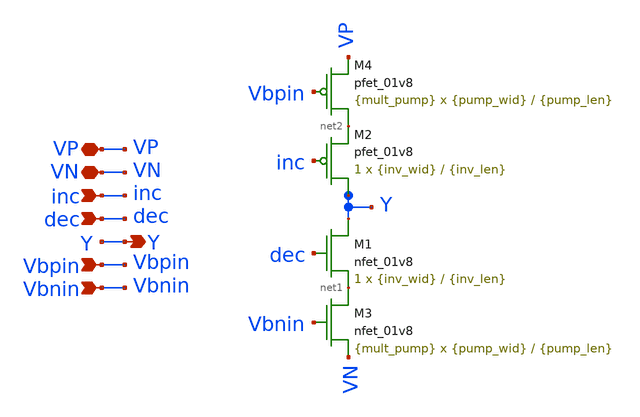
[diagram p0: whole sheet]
** sch_path: ipump.sch
**.subckt ipump VN VP Y Vbpin inc Vbnin dec
*.iopin VN
*.iopin VP
*.opin Y
*.ipin Vbpin
*.ipin inc
*.ipin Vbnin
*.ipin dec
XM1 Y dec net1 VN sky130_fd_pr__nfet_01v8 L={inv_len} W={inv_wid} nf=1 ad='int((nf+1)/2) * W/nf * 0.29'
+ as='int((nf+2)/2) * W/nf * 0.29' pd='2*int((nf+1)/2) * (W/nf + 0.29)' ps='2*int((nf+2)/2) * (W/nf + 0.29)'
+ nrd='0.29 / W' nrs='0.29 / W' sa=0 sb=0 sd=0 mult=1 m=1
XM2 Y inc net2 VP sky130_fd_pr__pfet_01v8 L={inv_len} W={inv_wid} nf=1 ad='int((nf+1)/2) * W/nf * 0.29'
+ as='int((nf+2)/2) * W/nf * 0.29' pd='2*int((nf+1)/2) * (W/nf + 0.29)' ps='2*int((nf+2)/2) * (W/nf + 0.29)'
+ nrd='0.29 / W' nrs='0.29 / W' sa=0 sb=0 sd=0 mult=1 m=1
XM3 net1 Vbnin VN VN sky130_fd_pr__nfet_01v8 L={pump_len} W={pump_wid} nf=1 ad='int((nf+1)/2) * W/nf * 0.29'
+ as='int((nf+2)/2) * W/nf * 0.29' pd='2*int((nf+1)/2) * (W/nf + 0.29)' ps='2*int((nf+2)/2) * (W/nf + 0.29)'
+ nrd='0.29 / W' nrs='0.29 / W' sa=0 sb=0 sd=0 mult={mult_pump} m={mult_pump}
XM4 net2 Vbpin VP VP sky130_fd_pr__pfet_01v8 L={pump_len} W={pump_wid} nf=1 ad='int((nf+1)/2) * W/nf * 0.29'
+ as='int((nf+2)/2) * W/nf * 0.29' pd='2*int((nf+1)/2) * (W/nf + 0.29)' ps='2*int((nf+2)/2) * (W/nf + 0.29)'
+ nrd='0.29 / W' nrs='0.29 / W' sa=0 sb=0 sd=0 mult={mult_pump} m={mult_pump}
**.ends
.end
